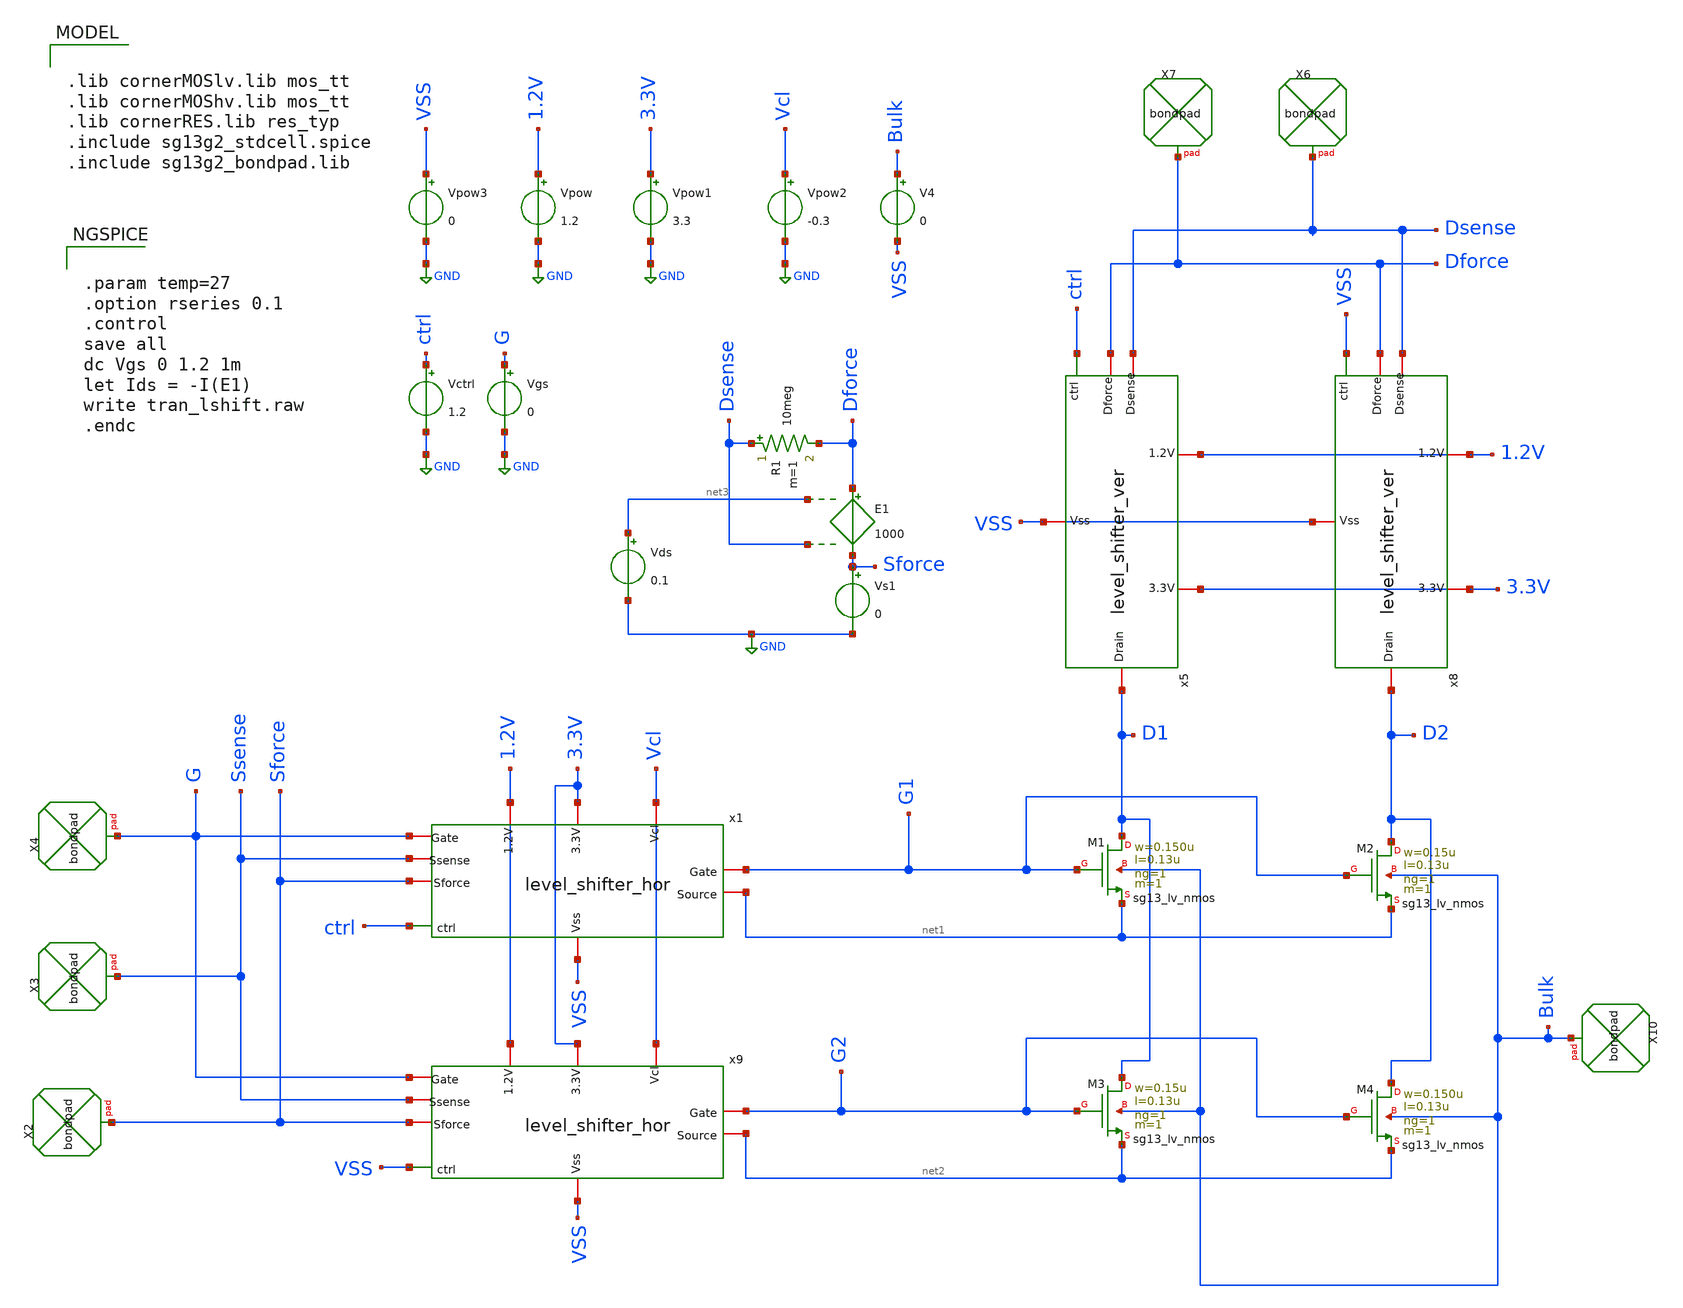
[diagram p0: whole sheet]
** sch_path: design_data/xschem/level_shifter_dc_smu_tb.sch
* Copyright 2023 IHP PDK Authors
* design_data/xschem/level_shifter_hor.sch:
* Copyright 2025 IHP PDK Authors
**.subckt level_shifter_dc_smu_tb
Vpow 1.2V GND 1.2
Vctrl ctrl GND 1.2
Vgs G GND 0
Vpow1 3.3V GND 3.3
Vpow2 Vcl GND -0.3
XX2 Sforce bondpad size=80u shape=0 padtype=0
XX3 Ssense bondpad size=80u shape=0 padtype=0
XX4 G bondpad size=80u shape=0 padtype=0
x1 1.2V Ssense Vcl ctrl net1 VSS 3.3V G1 G Sforce level_shifter_hor
x5 1.2V Dsense ctrl D1 VSS 3.3V Dforce level_shifter_ver
XX6 Dsense bondpad size=80u shape=0 padtype=0
XX7 Dforce bondpad size=80u shape=0 padtype=0
x8 1.2V Dsense VSS D2 VSS 3.3V Dforce level_shifter_ver
Vpow3 VSS GND 0
x9 1.2V Ssense Vcl VSS net2 VSS 3.3V G2 G Sforce level_shifter_hor
XX10 Bulk bondpad size=80u shape=0 padtype=0
XM1 D1 G1 net1 Bulk sg13_lv_nmos w=0.150u l=0.13u ng=1 m=1 mm_ok=1
XM2 D2 G1 net1 Bulk sg13_lv_nmos w=0.15u l=0.13u ng=1 m=1 mm_ok=1
XM3 D1 G2 net2 Bulk sg13_lv_nmos w=0.15u l=0.13u ng=1 m=1 mm_ok=1
XM4 D2 G2 net2 Bulk sg13_lv_nmos w=0.150u l=0.13u ng=1 m=1 mm_ok=1
V4 Bulk VSS 0
Vs1 Sforce GND 0
E1 Dforce Sforce net3 Dsense 1000
Vds net3 GND 0.1
R1 Dsense Dforce 10meg m=1
**** begin user architecture code

.lib cornerMOSlv.lib mos_tt
.lib cornerMOShv.lib mos_tt
.lib cornerRES.lib res_typ
.include sg13g2_stdcell.spice
.include sg13g2_bondpad.lib



.param temp=27
.option rseries 0.1
.control
save all
dc Vgs 0 1.2 1m
let Ids = -I(E1)
write tran_lshift.raw
.endc


**** end user architecture code
**.ends

* expanding   symbol:  level_shifter_hor.sym # of pins=10
** sym_path: design_data/xschem/level_shifter_hor.sym
** sch_path: design_data/xschem/level_shifter_hor.sch
.subckt level_shifter_hor 1.2V Ssense Vcl ctrl Source Vss 3.3V Gate G2 Sforce
*.iopin Gate
*.iopin Vss
*.iopin G2
*.iopin 3.3V
*.ipin ctrl
*.iopin 1.2V
*.iopin Vcl
*.iopin Ssense
*.iopin Source
*.iopin Sforce
XM2 net1 net3 3.3V 3.3V sg13_hv_pmos w=0.3u l=0.4u ng=1 m=1 mm_ok=1
XM3 net2 ctrl Vss Vss sg13_lv_nmos w=0.15u l=0.13u ng=1 m=1 mm_ok=1
XM5 net2 ctrl 1.2V 1.2V sg13_lv_pmos w=0.3u l=0.13u ng=1 m=1 mm_ok=1
XM1 net3 net1 3.3V 3.3V sg13_hv_pmos w=0.3u l=0.4u ng=1 m=1 mm_ok=1
XM4 Gate net3 G2 3.3V sg13_hv_pmos w=1.3u l=0.4u ng=1 m=1 mm_ok=1
XM8 G2 net1 Gate Vss sg13_hv_nmos w=1.3u l=0.45u ng=1 m=1 mm_ok=1
XM6 net3 net2 Vss Vss sg13_hv_nmos w=1.0u l=0.45u ng=1 m=1 mm_ok=1
XM7 net1 ctrl Vss Vss sg13_hv_nmos w=1.0u l=0.45u ng=1 m=1 mm_ok=1
XM9 Vcl net3 Gate Vss sg13_hv_nmos w=1.3u l=0.45u ng=1 m=1 mm_ok=1
XM12 Source net3 Sforce 3.3V sg13_hv_pmos w=16u l=0.4u ng=5 m=1 mm_ok=1
XM13 Sforce net1 Source Vss sg13_hv_nmos w=8u l=0.45u ng=5 m=1 mm_ok=1
XM10 Ssense net1 Source Vss sg13_hv_nmos w=0.3u l=0.45u ng=1 m=1 mm_ok=1
XM11 Source net3 Ssense 3.3V sg13_hv_pmos w=0.3u l=0.4u ng=1 m=1 mm_ok=1
.ends


* expanding   symbol:  level_shifter_ver.sym # of pins=7
** sym_path: design_data/xschem/level_shifter_ver.sym
** sch_path: design_data/xschem/level_shifter_ver.sch
.subckt level_shifter_ver 1.2V Dsense ctrl Drain Vss 3.3V Dforce
*.iopin Vss
*.iopin 3.3V
*.ipin ctrl
*.iopin 1.2V
*.iopin Dsense
*.iopin Drain
*.iopin Dforce
XM2 net1 net3 3.3V 3.3V sg13_hv_pmos w=0.3u l=0.4u ng=1 m=1 mm_ok=1
XM3 net2 ctrl Vss Vss sg13_lv_nmos w=0.15u l=0.13u ng=1 m=1 mm_ok=1
XM5 net2 ctrl 1.2V 1.2V sg13_lv_pmos w=0.30u l=0.13u ng=1 m=1 mm_ok=1
XM1 net3 net1 3.3V 3.3V sg13_hv_pmos w=0.3u l=0.4u ng=1 m=1 mm_ok=1
XM6 net3 net2 Vss Vss sg13_hv_nmos w=1.0u l=0.45u ng=1 m=1 mm_ok=1
XM7 net1 ctrl Vss Vss sg13_hv_nmos w=1.0u l=0.45u ng=1 m=1 mm_ok=1
XM12 Drain net3 Dforce 3.3V sg13_hv_pmos w=16u l=0.4u ng=5 m=1 mm_ok=1
XM13 Dforce net1 Drain Vss sg13_hv_nmos w=8u l=0.45u ng=5 m=1 mm_ok=1
XM4 Dsense net1 Drain Vss sg13_hv_nmos w=0.3u l=0.45u ng=1 m=1 mm_ok=1
XM8 Drain net3 Dsense 3.3V sg13_hv_pmos w=0.3u l=0.4u ng=1 m=1 mm_ok=1
.ends

.GLOBAL GND
.end
